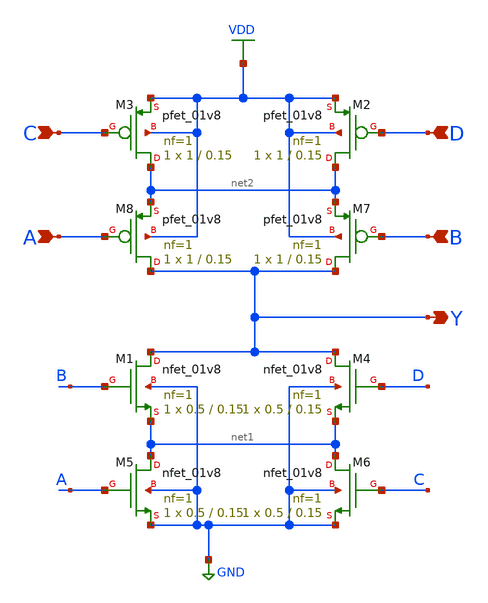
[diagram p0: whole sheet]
** sch_path: xschem/aoi22.sch
**.subckt aoi22 Y C A D B
*.opin Y
*.ipin C
*.ipin A
*.ipin D
*.ipin B
XM1 Y B net1 GND sky130_fd_pr__nfet_01v8 L=0.15 W=0.5 nf=1 ad='int((nf+1)/2) * W/nf * 0.29' as='int((nf+2)/2) * W/nf * 0.29'
+ pd='2*int((nf+1)/2) * (W/nf + 0.29)' ps='2*int((nf+2)/2) * (W/nf + 0.29)' nrd='0.29 / W' nrs='0.29 / W'
+ sa=0 sb=0 sd=0 mult=1 m=1
XM2 net2 D VDD VDD sky130_fd_pr__pfet_01v8 L=0.15 W=1 nf=1 ad='int((nf+1)/2) * W/nf * 0.29' as='int((nf+2)/2) * W/nf * 0.29'
+ pd='2*int((nf+1)/2) * (W/nf + 0.29)' ps='2*int((nf+2)/2) * (W/nf + 0.29)' nrd='0.29 / W' nrs='0.29 / W'
+ sa=0 sb=0 sd=0 mult=1 m=1
XM3 net2 C VDD VDD sky130_fd_pr__pfet_01v8 L=0.15 W=1 nf=1 ad='int((nf+1)/2) * W/nf * 0.29' as='int((nf+2)/2) * W/nf * 0.29'
+ pd='2*int((nf+1)/2) * (W/nf + 0.29)' ps='2*int((nf+2)/2) * (W/nf + 0.29)' nrd='0.29 / W' nrs='0.29 / W'
+ sa=0 sb=0 sd=0 mult=1 m=1
XM4 Y D net1 GND sky130_fd_pr__nfet_01v8 L=0.15 W=0.5 nf=1 ad='int((nf+1)/2) * W/nf * 0.29' as='int((nf+2)/2) * W/nf * 0.29'
+ pd='2*int((nf+1)/2) * (W/nf + 0.29)' ps='2*int((nf+2)/2) * (W/nf + 0.29)' nrd='0.29 / W' nrs='0.29 / W'
+ sa=0 sb=0 sd=0 mult=1 m=1
XM5 net1 A GND GND sky130_fd_pr__nfet_01v8 L=0.15 W=0.5 nf=1 ad='int((nf+1)/2) * W/nf * 0.29' as='int((nf+2)/2) * W/nf * 0.29'
+ pd='2*int((nf+1)/2) * (W/nf + 0.29)' ps='2*int((nf+2)/2) * (W/nf + 0.29)' nrd='0.29 / W' nrs='0.29 / W'
+ sa=0 sb=0 sd=0 mult=1 m=1
XM6 net1 C GND GND sky130_fd_pr__nfet_01v8 L=0.15 W=0.5 nf=1 ad='int((nf+1)/2) * W/nf * 0.29' as='int((nf+2)/2) * W/nf * 0.29'
+ pd='2*int((nf+1)/2) * (W/nf + 0.29)' ps='2*int((nf+2)/2) * (W/nf + 0.29)' nrd='0.29 / W' nrs='0.29 / W'
+ sa=0 sb=0 sd=0 mult=1 m=1
XM7 Y B net2 VDD sky130_fd_pr__pfet_01v8 L=0.15 W=1 nf=1 ad='int((nf+1)/2) * W/nf * 0.29' as='int((nf+2)/2) * W/nf * 0.29'
+ pd='2*int((nf+1)/2) * (W/nf + 0.29)' ps='2*int((nf+2)/2) * (W/nf + 0.29)' nrd='0.29 / W' nrs='0.29 / W'
+ sa=0 sb=0 sd=0 mult=1 m=1
XM8 Y A net2 VDD sky130_fd_pr__pfet_01v8 L=0.15 W=1 nf=1 ad='int((nf+1)/2) * W/nf * 0.29' as='int((nf+2)/2) * W/nf * 0.29'
+ pd='2*int((nf+1)/2) * (W/nf + 0.29)' ps='2*int((nf+2)/2) * (W/nf + 0.29)' nrd='0.29 / W' nrs='0.29 / W'
+ sa=0 sb=0 sd=0 mult=1 m=1
**.ends
.GLOBAL VDD
.GLOBAL GND
.end
